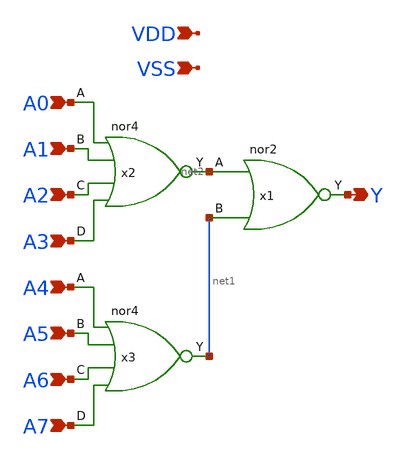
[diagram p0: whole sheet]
** sch_path: design/xschem/NOR/nor8.sch
**.subckt nor8 A0 A1 A2 A3 A4 A5 A6 A7 Y VDD VSS
*.ipin A0
*.ipin A1
*.ipin A2
*.ipin A3
*.ipin A4
*.ipin A5
*.ipin A6
*.ipin A7
*.opin Y
*.ipin VDD
*.ipin VSS
x2 A0 A1 A2 A3 VSS VDD net2 nor4
x3 A4 A5 A6 A7 VSS VDD net1 nor4
x1 net2 net1 VSS VDD Y nor2
**.ends
.end
